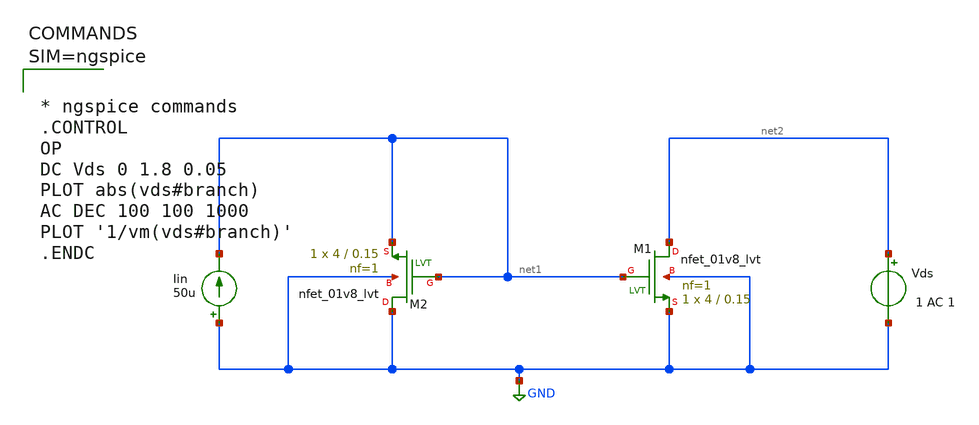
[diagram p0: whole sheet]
** sch_path: work/xschem/currentmirror.sch
**.subckt currentmirror
XM1 net2 net1 GND GND sky130_fd_pr__nfet_01v8_lvt L=0.15 W=4 nf=1 ad='int((1 + 1)/2) * 4 / 1 * 0.29'
+ as='int((1 + 2)/2) * 4 / 1 * 0.29' pd='2*int((1 + 1)/2) * (4 / 1 + 0.29)' ps='2*int((1 + 2)/2) * (4 / 1 + 0.29)'
+ nrd='0.29 / 4 ' nrs='0.29 / 4 ' sa=0 sb=0 sd=0 mult=1 m=1
Iin GND net1 50u
Vds net2 GND 1 AC 1
XM2 GND net1 net1 GND sky130_fd_pr__nfet_01v8_lvt L=0.15 W=4 nf=1 ad='int((1 + 1)/2) * 4 / 1 * 0.29'
+ as='int((1 + 2)/2) * 4 / 1 * 0.29' pd='2*int((1 + 1)/2) * (4 / 1 + 0.29)' ps='2*int((1 + 2)/2) * (4 / 1 + 0.29)'
+ nrd='0.29 / 4 ' nrs='0.29 / 4 ' sa=0 sb=0 sd=0 mult=1 m=1
**** begin user architecture code

** opencircuitdesign pdks install
.lib $::SKYWATER_MODELS/sky130.lib.spice tt




* ngspice commands
.CONTROL
OP
DC Vds 0 1.8 0.05
PLOT abs(vds#branch)
AC DEC 100 100 1000
PLOT '1/vm(vds#branch)'
.ENDC



**** end user architecture code
**.ends
.GLOBAL GND
.end
